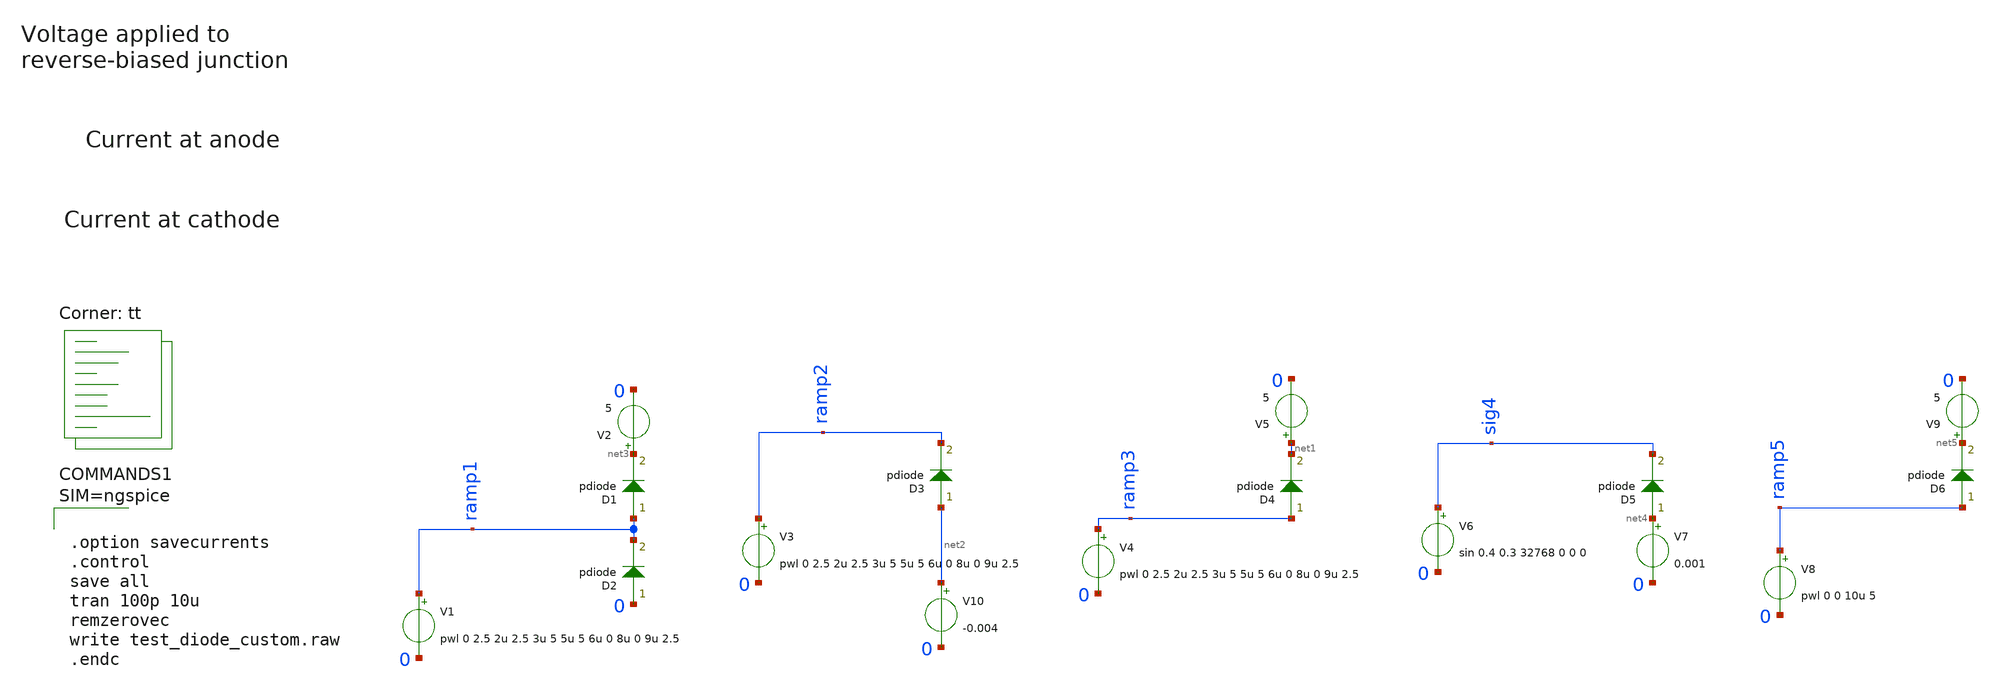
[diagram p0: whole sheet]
** sch_path: xschem/test_diode_custom.sch
* Copyright 2021 Stefan Frederik Schippers
* Licensed under the Apache License, Version 2.0 (the "License");
* you may not use this file except in compliance with the License.
* You may obtain a copy of the License at
* https://www.apache.org/licenses/LICENSE-2.0
* Unless required by applicable law or agreed to in writing, software
* distributed under the License is distributed on an "AS IS" BASIS,
* WITHOUT WARRANTIES OR CONDITIONS OF ANY KIND, either express or implied.
* See the License for the specific language governing permissions and
* limitations under the License.
**.subckt test_diode_custom
V4 ramp3 0 pwl 0 2.5 2u 2.5 3u 5 5u 5 6u 0 8u 0 9u 2.5
V5 net1 0 5
V3 ramp2 0 pwl 0 2.5 2u 2.5 3u 5 5u 5 6u 0 8u 0 9u 2.5
V2 net3 0 5
V1 ramp1 0 pwl 0 2.5 2u 2.5 3u 5 5u 5 6u 0 8u 0 9u 2.5
V7 net4 0 0.001
V6 sig4 0 sin 0.4 0.3 32768 0 0 0
V8 ramp5 0 pwl 0 0 10u 5
V9 net5 0 5
V10 net2 0 -0.004
D6 ramp5 net5 pdiode area=2.025e11
D1 ramp1 net3 pdiode area=2.025e11
D2 0 ramp1 pdiode area=2.025e11
D3 net2 ramp2 pdiode area=2.025e11
D4 ramp3 net1 pdiode area=2.025e11
D5 net4 sig4 pdiode area=2.025e11
**** begin user architecture code



.option savecurrents
.control
save all
tran 100p 10u
remzerovec
write test_diode_custom.raw
.endc



.lib $::SKYWATER_MODELS/sky130.lib.spice tt


*  Model parameters from sky130_fd_pr OpenPDK
*  sky130_fd_pr__diode_pd2nw_05v5
*  PPlus to Nwell normal Pmos VT Diode Model
*  -----------------------------------------------------

.model pdiode d   level = 3
*
*PARAMETERS TO MAKE MODEL INTO CADFLOW  tlevc = 1  area = 2.025e11  pj = 1.8e6
*
*JUNCTION CAPACITANCE PARAMETERS  cj = 1e-12  mj = 0.34629  pb = 0.6587  cjsw = 3.3e-013  mjsw =
*+ 0.29781  php = 0.7418  cta = 0.0012407  ctp = 0.00037357  tpb = 0.0020386  tphp = 0.001246
*
*DIODE IV PARAMETERS  js = 2.1483e-017  jsw = 8.04e-016  n = 1.3632  rs = 600e-12  ik = 4.76e4  ikr
*+ = 0  vb = 6000  ibv = 0.00106  trs = 0  eg = 1.05  xti = 5.2  tref = 30
*
*DEFAULT PARAMETERS  tcv = 0  gap1 = 0.000473  gap2 = 1110  ttt1 = 0  ttt2 = 0  tm1 = 0  tm2 = 0  lm
*+ = 0  lp = 0  wm = 0  wp = 0  xm = 0  xoi = 10000  xom = 10000  xp = 0  xw = 0


**** end user architecture code
**.ends
.end
